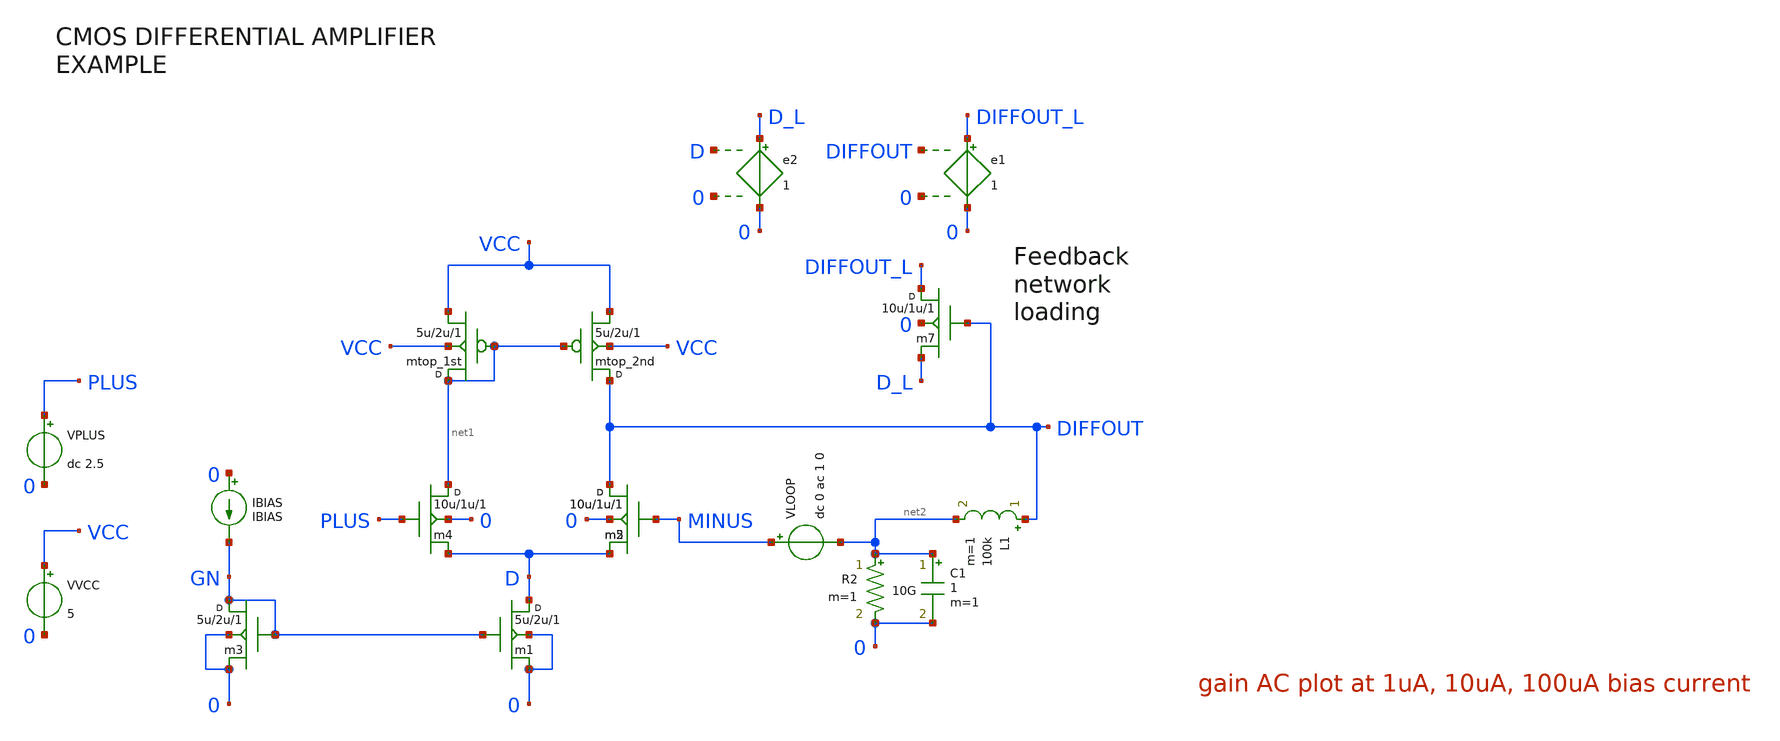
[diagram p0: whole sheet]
** sch_path: xschem_library/examples/test_ac.sch
**.subckt test_ac
m1 D GN 0 0 cmosn w=5u l=2u m=1
mtop_2nd DIFFOUT net1 VCC VCC cmosp w=5u l=2u m=1
VVCC VCC 0 5
m3 GN GN 0 0 cmosn w=5u l=2u m=1
IBIAS 0 GN IBIAS
m4 net1 PLUS D 0 cmosn w=10u l=1u m=1
m5 DIFFOUT MINUS D 0 cmosn w=10u l=1u m=1
mtop_1st net1 net1 VCC VCC cmosp w=5u l=2u m=1
VPLUS PLUS 0 dc 2.5
e1 DIFFOUT_L 0 DIFFOUT 0 1
e2 D_L 0 D 0 1
m7 DIFFOUT_L DIFFOUT D_L 0 cmosn w=10u l=1u m=1
VLOOP MINUS net2 dc 0 ac 1 0
R2 net2 0 10G m=1
L1 DIFFOUT net2 100k m=1
C1 net2 0 1 m=1
m2 DIFFOUT MINUS D 0 cmosn w=10u l=1u m=1
**** begin user architecture code


** ngspice
.temp 30

** models are generally not free: you must download
** SPICE models for active devices and put them  into the below
** referenced file in netlist/simulation directory.
** http://bwrcs.eecs.berkeley.edu/Classes/icdesign/ee241_s00/ASSIGNMENTS/TSMC035-n96g-params.txt
.include "models_cmos_example.txt"

.param IBIAS=1u
.control
let C=180/PI
ac dec 10 1000 10G
write test_ac.raw
set appendwrite
alter IBIAS=10u
ac dec 10 1000 10G
write test_ac.raw
alter IBIAS=100u
ac dec 10 1000 10G
write test_ac.raw
* plot vdb(ac1.diffout)
* plot C*phase(ac1.diffout)
* plot vdb(ac2.diffout)
* plot C*phase(ac2.diffout)
* plot vdb(ac3.diffout)
* plot C*phase(ac3.diffout)
.endc

** ngspice
* .save all

** xyce, not needed if -r given om cmdline
* .print tran format=raw v(diffout) v(plus) v(minus)


**** end user architecture code
**.ends
.end
